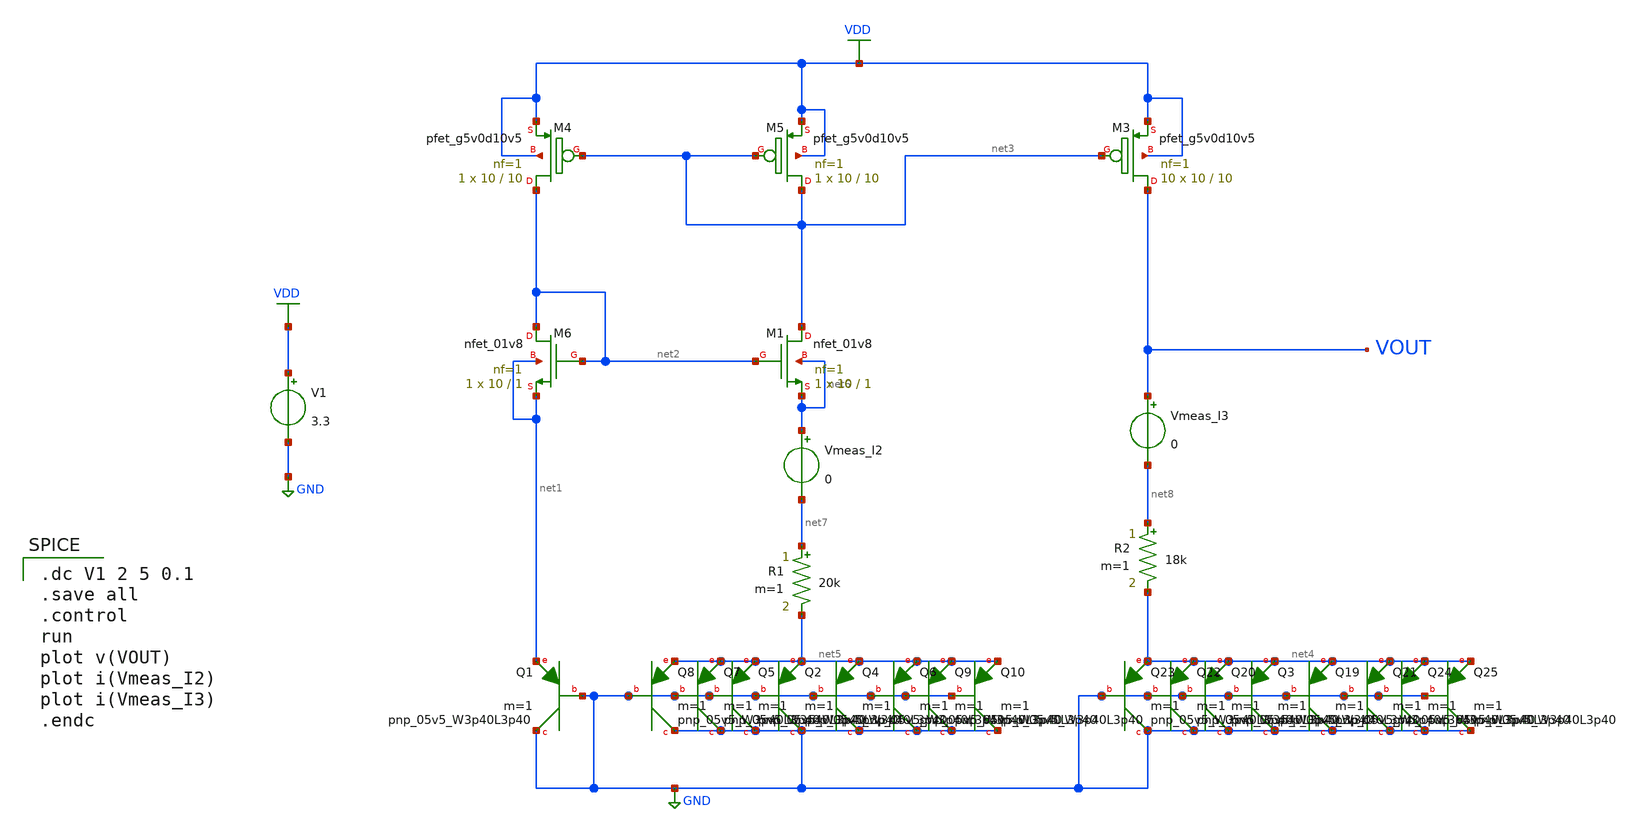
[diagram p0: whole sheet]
** sch_path: Circuits/Examples/Analog/BGR/BGR_BJT_1.2v.sch
**.subckt BGR_BJT_1.2v
XM4 net2 net3 VDD VDD sky130_fd_pr__pfet_g5v0d10v5 L=10 W=10 nf=1 ad='int((nf+1)/2) * W/nf * 0.29' as='int((nf+2)/2) * W/nf * 0.29'
+ pd='2*int((nf+1)/2) * (W/nf + 0.29)' ps='2*int((nf+2)/2) * (W/nf + 0.29)' nrd='0.29 / W' nrs='0.29 / W'
+ sa=0 sb=0 sd=0 mult=1 m=1
XM5 net3 net3 VDD VDD sky130_fd_pr__pfet_g5v0d10v5 L=10 W=10 nf=1 ad='int((nf+1)/2) * W/nf * 0.29' as='int((nf+2)/2) * W/nf * 0.29'
+ pd='2*int((nf+1)/2) * (W/nf + 0.29)' ps='2*int((nf+2)/2) * (W/nf + 0.29)' nrd='0.29 / W' nrs='0.29 / W'
+ sa=0 sb=0 sd=0 mult=1 m=1
R1 net7 net5 20k m=1
XM3 VOUT net3 VDD VDD sky130_fd_pr__pfet_g5v0d10v5 L=10 W=10 nf=1 ad='int((nf+1)/2) * W/nf * 0.29' as='int((nf+2)/2) * W/nf * 0.29'
+ pd='2*int((nf+1)/2) * (W/nf + 0.29)' ps='2*int((nf+2)/2) * (W/nf + 0.29)' nrd='0.29 / W' nrs='0.29 / W'
+ sa=0 sb=0 sd=0 mult=10 m=10
R2 net8 net4 18k m=1
V1 VDD GND 3.3
Vmeas_I2 net6 net7 0
Vmeas_I3 VOUT net8 0
XQ1 GND GND net1 sky130_fd_pr__pnp_05v5_W3p40L3p40 m=1
XQ2 GND GND net5 sky130_fd_pr__pnp_05v5_W3p40L3p40 m=1
XQ4 GND GND net5 sky130_fd_pr__pnp_05v5_W3p40L3p40 m=1
XQ5 GND GND net5 sky130_fd_pr__pnp_05v5_W3p40L3p40 m=1
XQ6 GND GND net5 sky130_fd_pr__pnp_05v5_W3p40L3p40 m=1
XQ7 GND GND net5 sky130_fd_pr__pnp_05v5_W3p40L3p40 m=1
XQ8 GND GND net5 sky130_fd_pr__pnp_05v5_W3p40L3p40 m=1
XQ9 GND GND net5 sky130_fd_pr__pnp_05v5_W3p40L3p40 m=1
XQ10 GND GND net5 sky130_fd_pr__pnp_05v5_W3p40L3p40 m=1
XQ3 GND GND net4 sky130_fd_pr__pnp_05v5_W3p40L3p40 m=1
XQ19 GND GND net4 sky130_fd_pr__pnp_05v5_W3p40L3p40 m=1
XQ20 GND GND net4 sky130_fd_pr__pnp_05v5_W3p40L3p40 m=1
XQ21 GND GND net4 sky130_fd_pr__pnp_05v5_W3p40L3p40 m=1
XQ22 GND GND net4 sky130_fd_pr__pnp_05v5_W3p40L3p40 m=1
XQ23 GND GND net4 sky130_fd_pr__pnp_05v5_W3p40L3p40 m=1
XQ24 GND GND net4 sky130_fd_pr__pnp_05v5_W3p40L3p40 m=1
XQ25 GND GND net4 sky130_fd_pr__pnp_05v5_W3p40L3p40 m=1
XM6 net2 net2 net1 net1 sky130_fd_pr__nfet_01v8 L=1 W=10 nf=1 ad='int((nf+1)/2) * W/nf * 0.29' as='int((nf+2)/2) * W/nf * 0.29'
+ pd='2*int((nf+1)/2) * (W/nf + 0.29)' ps='2*int((nf+2)/2) * (W/nf + 0.29)' nrd='0.29 / W' nrs='0.29 / W'
+ sa=0 sb=0 sd=0 mult=1 m=1
XM1 net3 net2 net6 net6 sky130_fd_pr__nfet_01v8 L=1 W=10 nf=1 ad='int((nf+1)/2) * W/nf * 0.29' as='int((nf+2)/2) * W/nf * 0.29'
+ pd='2*int((nf+1)/2) * (W/nf + 0.29)' ps='2*int((nf+2)/2) * (W/nf + 0.29)' nrd='0.29 / W' nrs='0.29 / W'
+ sa=0 sb=0 sd=0 mult=1 m=1
**** begin user architecture code

.dc V1 2 5 0.1
.save all
.control
run
plot v(VOUT)
plot i(Vmeas_I2)
plot i(Vmeas_I3)
.endc


 ** manual skywater pdks install (with patches applied)
* .lib $::SKYWATER_MODELS/models/sky130.lib.spice tt

** opencircuitdesign pdks install
.lib $::SKYWATER_MODELS/sky130.lib.spice tt

** manual skywater-pdk install (with patches applied).
* .include $::SKYWATER_MODELS/cells/pnp_05v5/sky130_fd_pr__pnp_05v5_W3p40L3p40.model.spice

** opencircuitdesign pdks install
.include ~/OpenPDK/open_pdks/sky130/sky130A/libs.ref/sky130_fd_pr/spice/sky130_fd_pr__pnp_05v5_W3p40L3p40.model.spice
*.include $::SKYWATER_MODELS/../../libs.ref/sky130_fd_pr/spice/sky130_fd_pr__pnp_05v5_W3p40L3p40.model.spice

.param mc_mm_switch=0
.param mc_pr_switch=1

**** end user architecture code
**.ends
.GLOBAL GND
.GLOBAL VDD
.end
